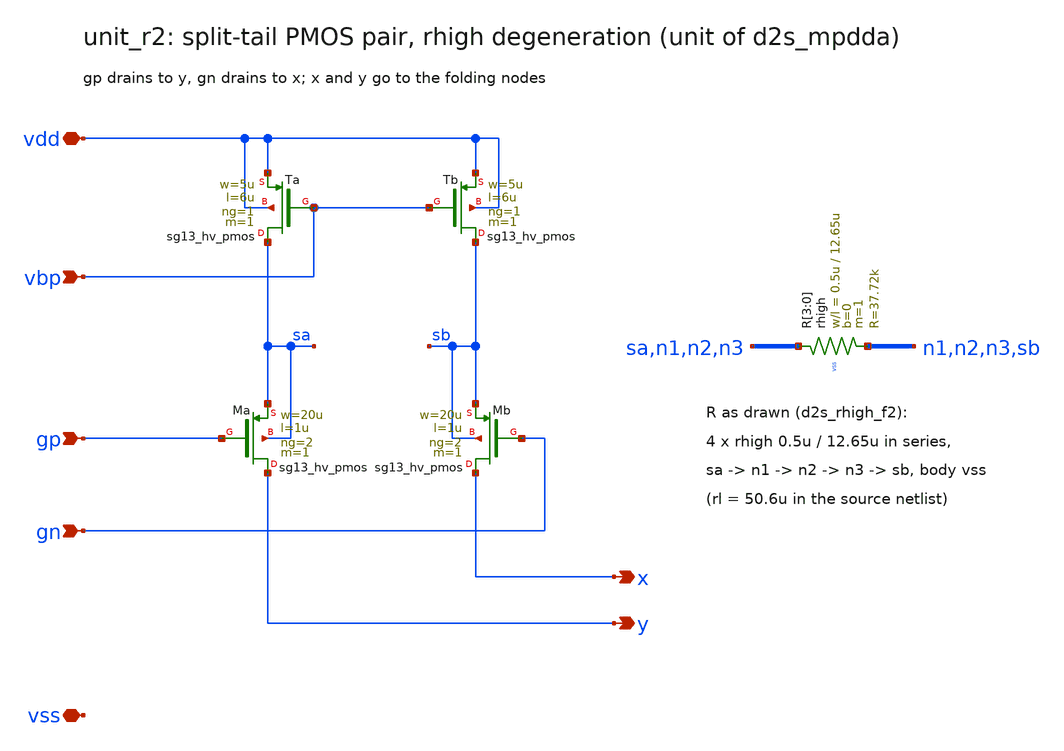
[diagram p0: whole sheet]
** sch_path: macros/sg13cmos5l_IOPadDiff2Single/schematic/xschem/unit_r2.sch
**.subckt unit_r2 x y gp gn vdd vss vbp
*.opin x
*.opin y
*.ipin gp
*.ipin gn
*.iopin vdd
*.iopin vss
*.ipin vbp
XTa sa vbp vdd vdd sg13_hv_pmos w=5u l=6u ng=1 m=1 mm_ok=1
XTb sb vbp vdd vdd sg13_hv_pmos w=5u l=6u ng=1 m=1 mm_ok=1
XMa y gp sa sa sg13_hv_pmos w=20u l=1u ng=2 m=1 mm_ok=1
XMb x gn sb sb sg13_hv_pmos w=20u l=1u ng=2 m=1 mm_ok=1
XR[3] sa n1 vss rhigh w=0.5u l=12.65u m=1 b=0 mm_ok=1
XR[2] n1 n2 vss rhigh w=0.5u l=12.65u m=1 b=0 mm_ok=1
XR[1] n2 n3 vss rhigh w=0.5u l=12.65u m=1 b=0 mm_ok=1
XR[0] n3 sb vss rhigh w=0.5u l=12.65u m=1 b=0 mm_ok=1
**.ends
.end
